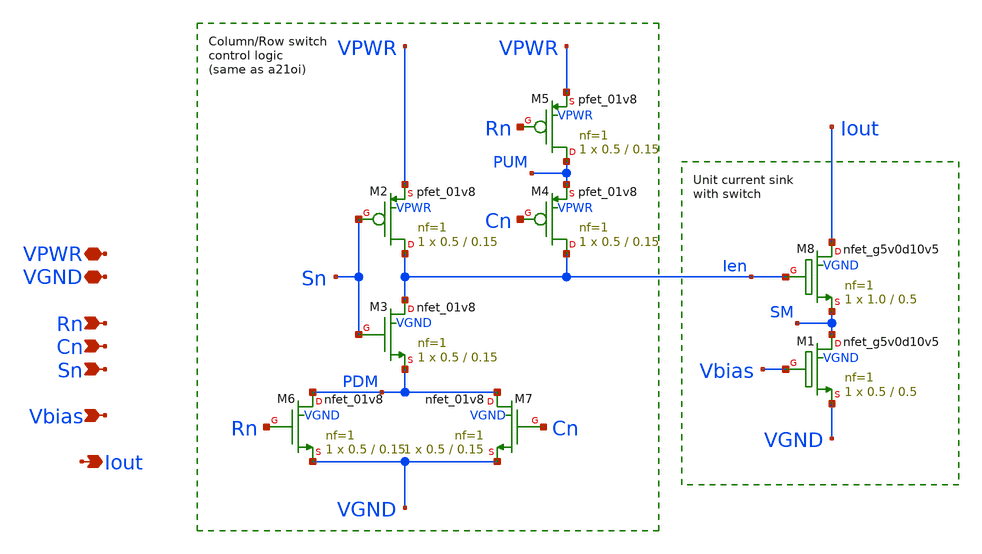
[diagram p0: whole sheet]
** sch_path: xschem/icell.sch
**.subckt icell Rn VPWR Iout VGND Cn Sn Vbias
*.ipin Rn
*.iopin VPWR
*.opin Iout
*.iopin VGND
*.ipin Cn
*.ipin Sn
*.ipin Vbias
XM2 Ien Sn VPWR VPWR sky130_fd_pr__pfet_01v8 L=0.15 W=0.5 nf=1 ad='int((nf+1)/2) * W/nf * 0.29' as='int((nf+2)/2) * W/nf * 0.29'
+ pd='2*int((nf+1)/2) * (W/nf + 0.29)' ps='2*int((nf+2)/2) * (W/nf + 0.29)' nrd='0.29 / W' nrs='0.29 / W'
+ sa=0 sb=0 sd=0 mult=1 m=1
XM3 Ien Sn PDM VGND sky130_fd_pr__nfet_01v8 L=0.15 W=0.5 nf=1 ad='int((nf+1)/2) * W/nf * 0.29' as='int((nf+2)/2) * W/nf * 0.29'
+ pd='2*int((nf+1)/2) * (W/nf + 0.29)' ps='2*int((nf+2)/2) * (W/nf + 0.29)' nrd='0.29 / W' nrs='0.29 / W'
+ sa=0 sb=0 sd=0 mult=1 m=1
XM4 Ien Cn PUM VPWR sky130_fd_pr__pfet_01v8 L=0.15 W=0.5 nf=1 ad='int((nf+1)/2) * W/nf * 0.29' as='int((nf+2)/2) * W/nf * 0.29'
+ pd='2*int((nf+1)/2) * (W/nf + 0.29)' ps='2*int((nf+2)/2) * (W/nf + 0.29)' nrd='0.29 / W' nrs='0.29 / W'
+ sa=0 sb=0 sd=0 mult=1 m=1
XM5 PUM Rn VPWR VPWR sky130_fd_pr__pfet_01v8 L=0.15 W=0.5 nf=1 ad='int((nf+1)/2) * W/nf * 0.29' as='int((nf+2)/2) * W/nf * 0.29'
+ pd='2*int((nf+1)/2) * (W/nf + 0.29)' ps='2*int((nf+2)/2) * (W/nf + 0.29)' nrd='0.29 / W' nrs='0.29 / W'
+ sa=0 sb=0 sd=0 mult=1 m=1
XM6 PDM Rn VGND VGND sky130_fd_pr__nfet_01v8 L=0.15 W=0.5 nf=1 ad='int((nf+1)/2) * W/nf * 0.29' as='int((nf+2)/2) * W/nf * 0.29'
+ pd='2*int((nf+1)/2) * (W/nf + 0.29)' ps='2*int((nf+2)/2) * (W/nf + 0.29)' nrd='0.29 / W' nrs='0.29 / W'
+ sa=0 sb=0 sd=0 mult=1 m=1
XM7 PDM Cn VGND VGND sky130_fd_pr__nfet_01v8 L=0.15 W=0.5 nf=1 ad='int((nf+1)/2) * W/nf * 0.29' as='int((nf+2)/2) * W/nf * 0.29'
+ pd='2*int((nf+1)/2) * (W/nf + 0.29)' ps='2*int((nf+2)/2) * (W/nf + 0.29)' nrd='0.29 / W' nrs='0.29 / W'
+ sa=0 sb=0 sd=0 mult=1 m=1
XM1 SM Vbias VGND VGND sky130_fd_pr__nfet_g5v0d10v5 L=0.5 W=0.5 nf=1 ad='int((nf+1)/2) * W/nf * 0.29'
+ as='int((nf+2)/2) * W/nf * 0.29' pd='2*int((nf+1)/2) * (W/nf + 0.29)' ps='2*int((nf+2)/2) * (W/nf + 0.29)'
+ nrd='0.29 / W' nrs='0.29 / W' sa=0 sb=0 sd=0 mult=1 m=1
XM8 Iout Ien SM VGND sky130_fd_pr__nfet_g5v0d10v5 L=0.5 W=1.0 nf=1 ad='int((nf+1)/2) * W/nf * 0.29' as='int((nf+2)/2) * W/nf * 0.29'
+ pd='2*int((nf+1)/2) * (W/nf + 0.29)' ps='2*int((nf+2)/2) * (W/nf + 0.29)' nrd='0.29 / W' nrs='0.29 / W'
+ sa=0 sb=0 sd=0 mult=1 m=1
**.ends
.end
